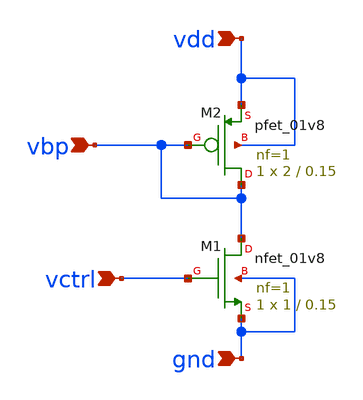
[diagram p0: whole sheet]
** sch_path: vcro/vbias.sch
**.subckt vbias vbp vctrl vdd gnd
*.ipin vbp
*.ipin vctrl
*.ipin vdd
*.ipin gnd
XM1 vbp vctrl gnd gnd sky130_fd_pr__nfet_01v8 L=0.15 W=1 nf=1 ad='int((1 + 1)/2) * 1 / 1 * 0.29' as='int((1 + 2)/2) * 1 / 1 * 0.29'
+ pd='2*int((1 + 1)/2) * (1 / 1 + 0.29)' ps='2*int((1 + 2)/2) * (1 / 1 + 0.29)' nrd='0.29 / 1 ' nrs='0.29 / 1 '
+ sa=0 sb=0 sd=0 mult=1 m=1
XM2 vbp vbp vdd vdd sky130_fd_pr__pfet_01v8 L=0.15 W=2 nf=1 ad='int((1 + 1)/2) * 2 / 1 * 0.29' as='int((1 + 2)/2) * 2 / 1 * 0.29'
+ pd='2*int((1 + 1)/2) * (2 / 1 + 0.29)' ps='2*int((1 + 2)/2) * (2 / 1 + 0.29)' nrd='0.29 / 2 ' nrs='0.29 / 2 '
+ sa=0 sb=0 sd=0 mult=1 m=1
**.ends
.end
